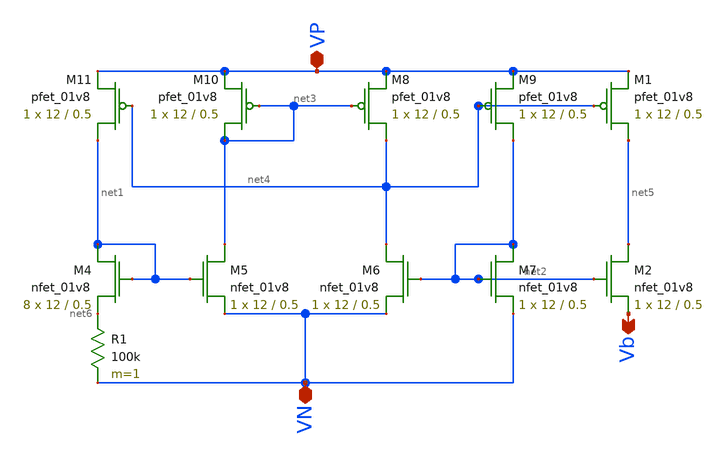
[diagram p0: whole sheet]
** sch_path: schematics/bias/current_bias.sch
**.subckt current_bias VP VN Vb
*.iopin VP
*.iopin VN
*.opin Vb
XM4 net1 net1 net6 GND sky130_fd_pr__nfet_01v8 L=0.5 W=12 nf=1 ad='int((nf+1)/2) * W/nf * 0.29' as='int((nf+2)/2) * W/nf * 0.29'
+ pd='2*int((nf+1)/2) * (W/nf + 0.29)' ps='2*int((nf+2)/2) * (W/nf + 0.29)' nrd='0.29 / W' nrs='0.29 / W'
+ sa=0 sb=0 sd=0 mult=8 m=8
XM5 net3 net1 VN GND sky130_fd_pr__nfet_01v8 L=0.5 W=12 nf=1 ad='int((nf+1)/2) * W/nf * 0.29' as='int((nf+2)/2) * W/nf * 0.29'
+ pd='2*int((nf+1)/2) * (W/nf + 0.29)' ps='2*int((nf+2)/2) * (W/nf + 0.29)' nrd='0.29 / W' nrs='0.29 / W'
+ sa=0 sb=0 sd=0 mult=1 m=1
XM6 net4 net2 VN GND sky130_fd_pr__nfet_01v8 L=0.5 W=12 nf=1 ad='int((nf+1)/2) * W/nf * 0.29' as='int((nf+2)/2) * W/nf * 0.29'
+ pd='2*int((nf+1)/2) * (W/nf + 0.29)' ps='2*int((nf+2)/2) * (W/nf + 0.29)' nrd='0.29 / W' nrs='0.29 / W'
+ sa=0 sb=0 sd=0 mult=1 m=1
XM7 net2 net2 VN GND sky130_fd_pr__nfet_01v8 L=0.5 W=12 nf=1 ad='int((nf+1)/2) * W/nf * 0.29' as='int((nf+2)/2) * W/nf * 0.29'
+ pd='2*int((nf+1)/2) * (W/nf + 0.29)' ps='2*int((nf+2)/2) * (W/nf + 0.29)' nrd='0.29 / W' nrs='0.29 / W'
+ sa=0 sb=0 sd=0 mult=1 m=1
R1 net6 VN 100k m=1
XM8 net4 net3 VP VDD sky130_fd_pr__pfet_01v8 L=0.5 W=12 nf=1 ad='int((nf+1)/2) * W/nf * 0.29' as='int((nf+2)/2) * W/nf * 0.29'
+ pd='2*int((nf+1)/2) * (W/nf + 0.29)' ps='2*int((nf+2)/2) * (W/nf + 0.29)' nrd='0.29 / W' nrs='0.29 / W'
+ sa=0 sb=0 sd=0 mult=1 m=1
XM9 net2 net4 VP VDD sky130_fd_pr__pfet_01v8 L=0.5 W=12 nf=1 ad='int((nf+1)/2) * W/nf * 0.29' as='int((nf+2)/2) * W/nf * 0.29'
+ pd='2*int((nf+1)/2) * (W/nf + 0.29)' ps='2*int((nf+2)/2) * (W/nf + 0.29)' nrd='0.29 / W' nrs='0.29 / W'
+ sa=0 sb=0 sd=0 mult=1 m=1
XM10 net3 net3 VP VDD sky130_fd_pr__pfet_01v8 L=0.5 W=12 nf=1 ad='int((nf+1)/2) * W/nf * 0.29' as='int((nf+2)/2) * W/nf * 0.29'
+ pd='2*int((nf+1)/2) * (W/nf + 0.29)' ps='2*int((nf+2)/2) * (W/nf + 0.29)' nrd='0.29 / W' nrs='0.29 / W'
+ sa=0 sb=0 sd=0 mult=1 m=1
XM11 net1 net4 VP VDD sky130_fd_pr__pfet_01v8 L=0.5 W=12 nf=1 ad='int((nf+1)/2) * W/nf * 0.29' as='int((nf+2)/2) * W/nf * 0.29'
+ pd='2*int((nf+1)/2) * (W/nf + 0.29)' ps='2*int((nf+2)/2) * (W/nf + 0.29)' nrd='0.29 / W' nrs='0.29 / W'
+ sa=0 sb=0 sd=0 mult=1 m=1
XM1 net5 net4 VP VDD sky130_fd_pr__pfet_01v8 L=0.5 W=12 nf=1 ad='int((nf+1)/2) * W/nf * 0.29' as='int((nf+2)/2) * W/nf * 0.29'
+ pd='2*int((nf+1)/2) * (W/nf + 0.29)' ps='2*int((nf+2)/2) * (W/nf + 0.29)' nrd='0.29 / W' nrs='0.29 / W'
+ sa=0 sb=0 sd=0 mult=1 m=1
XM2 net5 net2 Vb GND sky130_fd_pr__nfet_01v8 L=0.5 W=12 nf=1 ad='int((nf+1)/2) * W/nf * 0.29' as='int((nf+2)/2) * W/nf * 0.29'
+ pd='2*int((nf+1)/2) * (W/nf + 0.29)' ps='2*int((nf+2)/2) * (W/nf + 0.29)' nrd='0.29 / W' nrs='0.29 / W'
+ sa=0 sb=0 sd=0 mult=1 m=1
**.ends
.end
